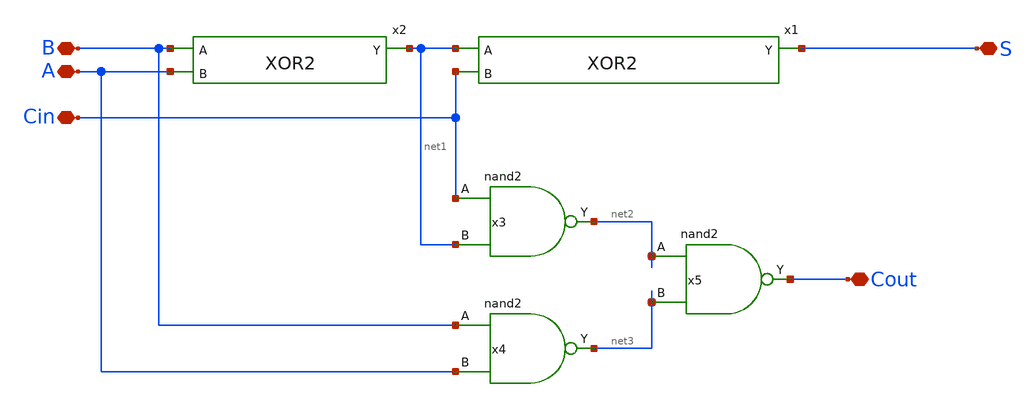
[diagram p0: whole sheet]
** sch_path: design/xschem/ADDER/full_adder.sch
**.subckt full_adder A B Cin S Cout
*.iopin A
*.iopin B
*.iopin Cin
*.iopin S
*.iopin Cout
x2 B A net1 VSS VDD XOR2
x1 net1 Cin S VSS VDD XOR2
x3 Cin net1 VSS VDD net2 nand2
x4 B A VSS VDD net3 nand2
x5 net2 net3 VSS VDD Cout nand2
**.ends
.end
